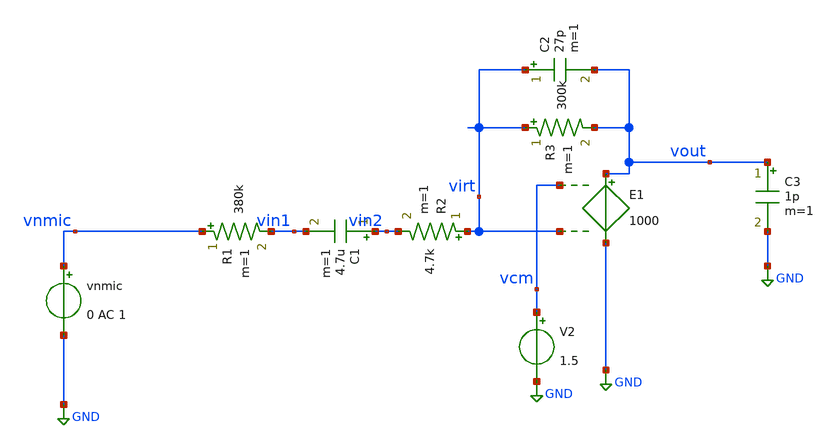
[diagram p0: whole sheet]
** sch_path: xschem/mytest.sch
**.subckt mytest
vnmic vnmic GND 0 AC 1
R1 vnmic vin1 380k m=1
C1 vin2 vin1 4.7u m=1
R2 virt vin2 4.7k m=1
E1 vout GND vcm virt 1000
R3 virt vout 300k m=1
C2 virt vout 27p m=1
V2 vcm GND 1.5
C3 vout GND 1p m=1
**.ends
.GLOBAL GND
.end
